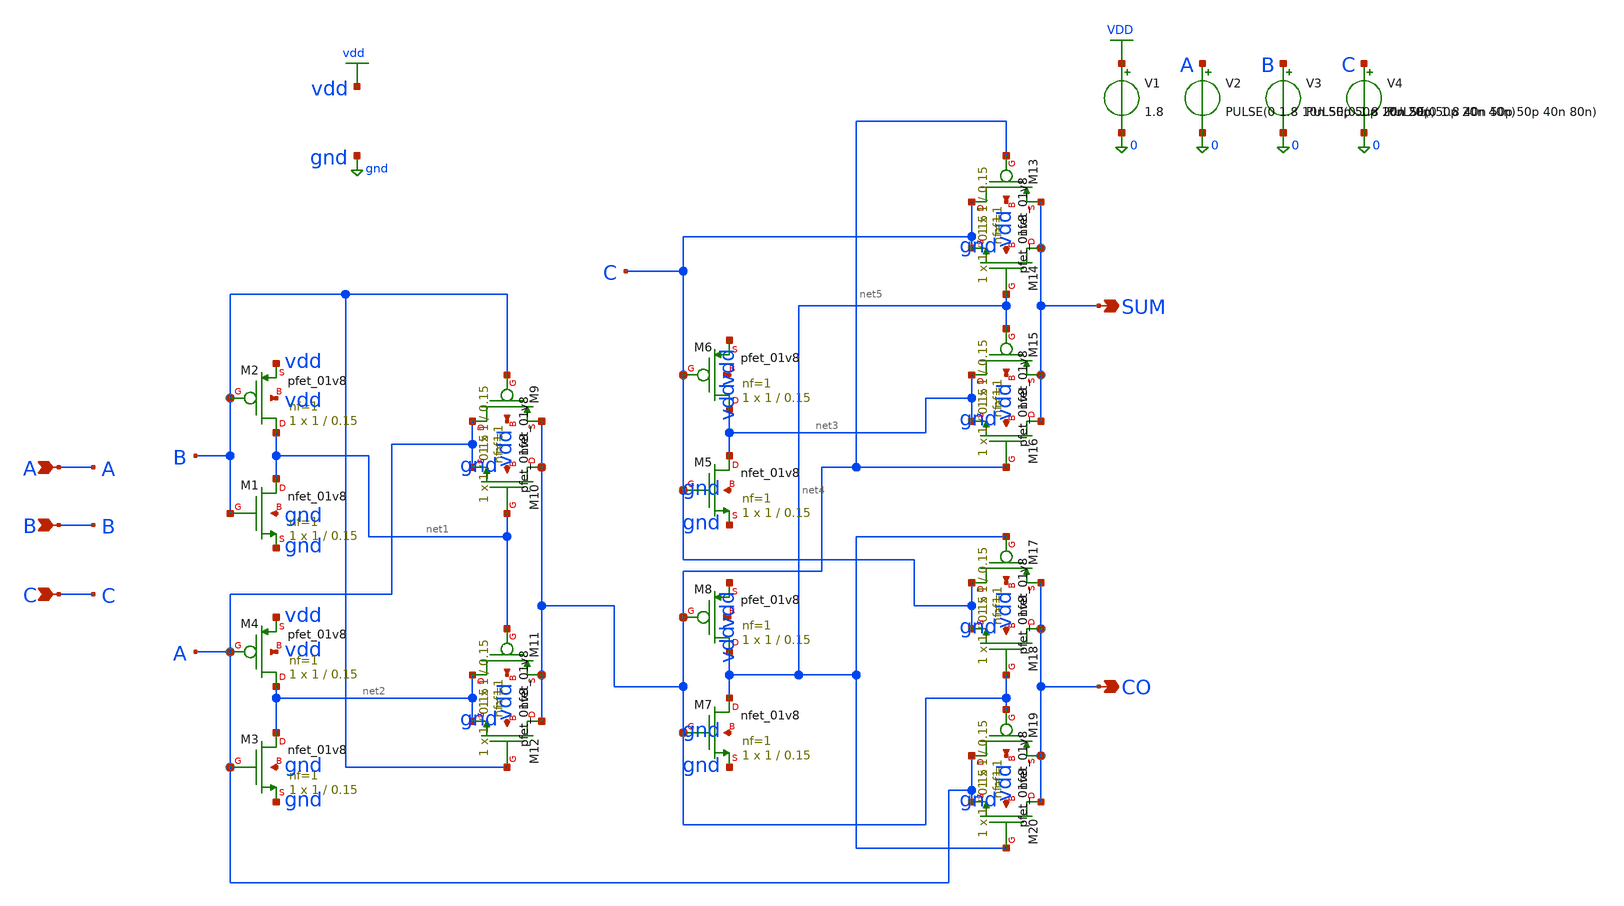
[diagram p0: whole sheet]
** sch_path: tb_FA20T.sch
**.subckt tb_FA20T A B C SUM CO
*.ipin A
*.ipin B
*.ipin C
*.opin SUM
*.opin CO
XM1 net1 B gnd gnd sky130_fd_pr__nfet_01v8 L=0.15 W=1 nf=1 ad='int((1 + 1)/2) * 1 / 1 * 0.29' as='int((1 + 2)/2) * 1 / 1 * 0.29'
+ pd='2*int((1 + 1)/2) * (1 / 1 + 0.29)' ps='2*int((1 + 2)/2) * (1 / 1 + 0.29)' nrd='0.29 / 1 ' nrs='0.29 / 1 '
+ sa=0 sb=0 sd=0 mult=1 m=1
XM2 net1 B vdd vdd sky130_fd_pr__pfet_01v8 L=0.15 W=1 nf=1 ad='int((1 + 1)/2) * 1 / 1 * 0.29' as='int((1 + 2)/2) * 1 / 1 * 0.29'
+ pd='2*int((1 + 1)/2) * (1 / 1 + 0.29)' ps='2*int((1 + 2)/2) * (1 / 1 + 0.29)' nrd='0.29 / 1 ' nrs='0.29 / 1 '
+ sa=0 sb=0 sd=0 mult=1 m=1
XM3 net2 A gnd gnd sky130_fd_pr__nfet_01v8 L=0.15 W=1 nf=1 ad='int((1 + 1)/2) * 1 / 1 * 0.29' as='int((1 + 2)/2) * 1 / 1 * 0.29'
+ pd='2*int((1 + 1)/2) * (1 / 1 + 0.29)' ps='2*int((1 + 2)/2) * (1 / 1 + 0.29)' nrd='0.29 / 1 ' nrs='0.29 / 1 '
+ sa=0 sb=0 sd=0 mult=1 m=1
XM4 net2 A vdd vdd sky130_fd_pr__pfet_01v8 L=0.15 W=1 nf=1 ad='int((1 + 1)/2) * 1 / 1 * 0.29' as='int((1 + 2)/2) * 1 / 1 * 0.29'
+ pd='2*int((1 + 1)/2) * (1 / 1 + 0.29)' ps='2*int((1 + 2)/2) * (1 / 1 + 0.29)' nrd='0.29 / 1 ' nrs='0.29 / 1 '
+ sa=0 sb=0 sd=0 mult=1 m=1
XM5 net3 C gnd gnd sky130_fd_pr__nfet_01v8 L=0.15 W=1 nf=1 ad='int((1 + 1)/2) * 1 / 1 * 0.29' as='int((1 + 2)/2) * 1 / 1 * 0.29'
+ pd='2*int((1 + 1)/2) * (1 / 1 + 0.29)' ps='2*int((1 + 2)/2) * (1 / 1 + 0.29)' nrd='0.29 / 1 ' nrs='0.29 / 1 '
+ sa=0 sb=0 sd=0 mult=1 m=1
XM6 net3 C vdd vdd sky130_fd_pr__pfet_01v8 L=0.15 W=1 nf=1 ad='int((1 + 1)/2) * 1 / 1 * 0.29' as='int((1 + 2)/2) * 1 / 1 * 0.29'
+ pd='2*int((1 + 1)/2) * (1 / 1 + 0.29)' ps='2*int((1 + 2)/2) * (1 / 1 + 0.29)' nrd='0.29 / 1 ' nrs='0.29 / 1 '
+ sa=0 sb=0 sd=0 mult=1 m=1
XM7 net4 net5 gnd gnd sky130_fd_pr__nfet_01v8 L=0.15 W=1 nf=1 ad='int((1 + 1)/2) * 1 / 1 * 0.29' as='int((1 + 2)/2) * 1 / 1 * 0.29'
+ pd='2*int((1 + 1)/2) * (1 / 1 + 0.29)' ps='2*int((1 + 2)/2) * (1 / 1 + 0.29)' nrd='0.29 / 1 ' nrs='0.29 / 1 '
+ sa=0 sb=0 sd=0 mult=1 m=1
XM8 net4 net5 vdd vdd sky130_fd_pr__pfet_01v8 L=0.15 W=1 nf=1 ad='int((1 + 1)/2) * 1 / 1 * 0.29' as='int((1 + 2)/2) * 1 / 1 * 0.29'
+ pd='2*int((1 + 1)/2) * (1 / 1 + 0.29)' ps='2*int((1 + 2)/2) * (1 / 1 + 0.29)' nrd='0.29 / 1 ' nrs='0.29 / 1 '
+ sa=0 sb=0 sd=0 mult=1 m=1
XM9 A B net5 vdd sky130_fd_pr__pfet_01v8 L=0.15 W=1 nf=1 ad='int((1 + 1)/2) * 1 / 1 * 0.29' as='int((1 + 2)/2) * 1 / 1 * 0.29'
+ pd='2*int((1 + 1)/2) * (1 / 1 + 0.29)' ps='2*int((1 + 2)/2) * (1 / 1 + 0.29)' nrd='0.29 / 1 ' nrs='0.29 / 1 '
+ sa=0 sb=0 sd=0 mult=1 m=1
XM10 net5 net1 A gnd sky130_fd_pr__nfet_01v8 L=0.15 W=1 nf=1 ad='int((1 + 1)/2) * 1 / 1 * 0.29' as='int((1 + 2)/2) * 1 / 1 * 0.29'
+ pd='2*int((1 + 1)/2) * (1 / 1 + 0.29)' ps='2*int((1 + 2)/2) * (1 / 1 + 0.29)' nrd='0.29 / 1 ' nrs='0.29 / 1 '
+ sa=0 sb=0 sd=0 mult=1 m=1
XM11 net2 net1 net5 vdd sky130_fd_pr__pfet_01v8 L=0.15 W=1 nf=1 ad='int((1 + 1)/2) * 1 / 1 * 0.29' as='int((1 + 2)/2) * 1 / 1 * 0.29'
+ pd='2*int((1 + 1)/2) * (1 / 1 + 0.29)' ps='2*int((1 + 2)/2) * (1 / 1 + 0.29)' nrd='0.29 / 1 ' nrs='0.29 / 1 '
+ sa=0 sb=0 sd=0 mult=1 m=1
XM12 net5 B net2 gnd sky130_fd_pr__nfet_01v8 L=0.15 W=1 nf=1 ad='int((1 + 1)/2) * 1 / 1 * 0.29' as='int((1 + 2)/2) * 1 / 1 * 0.29'
+ pd='2*int((1 + 1)/2) * (1 / 1 + 0.29)' ps='2*int((1 + 2)/2) * (1 / 1 + 0.29)' nrd='0.29 / 1 ' nrs='0.29 / 1 '
+ sa=0 sb=0 sd=0 mult=1 m=1
XM13 C net5 SUM vdd sky130_fd_pr__pfet_01v8 L=0.15 W=1 nf=1 ad='int((1 + 1)/2) * 1 / 1 * 0.29' as='int((1 + 2)/2) * 1 / 1 * 0.29'
+ pd='2*int((1 + 1)/2) * (1 / 1 + 0.29)' ps='2*int((1 + 2)/2) * (1 / 1 + 0.29)' nrd='0.29 / 1 ' nrs='0.29 / 1 '
+ sa=0 sb=0 sd=0 mult=1 m=1
XM14 SUM net4 C gnd sky130_fd_pr__nfet_01v8 L=0.15 W=1 nf=1 ad='int((1 + 1)/2) * 1 / 1 * 0.29' as='int((1 + 2)/2) * 1 / 1 * 0.29'
+ pd='2*int((1 + 1)/2) * (1 / 1 + 0.29)' ps='2*int((1 + 2)/2) * (1 / 1 + 0.29)' nrd='0.29 / 1 ' nrs='0.29 / 1 '
+ sa=0 sb=0 sd=0 mult=1 m=1
XM15 net3 net4 SUM vdd sky130_fd_pr__pfet_01v8 L=0.15 W=1 nf=1 ad='int((1 + 1)/2) * 1 / 1 * 0.29' as='int((1 + 2)/2) * 1 / 1 * 0.29'
+ pd='2*int((1 + 1)/2) * (1 / 1 + 0.29)' ps='2*int((1 + 2)/2) * (1 / 1 + 0.29)' nrd='0.29 / 1 ' nrs='0.29 / 1 '
+ sa=0 sb=0 sd=0 mult=1 m=1
XM16 SUM net5 net3 gnd sky130_fd_pr__nfet_01v8 L=0.15 W=1 nf=1 ad='int((1 + 1)/2) * 1 / 1 * 0.29' as='int((1 + 2)/2) * 1 / 1 * 0.29'
+ pd='2*int((1 + 1)/2) * (1 / 1 + 0.29)' ps='2*int((1 + 2)/2) * (1 / 1 + 0.29)' nrd='0.29 / 1 ' nrs='0.29 / 1 '
+ sa=0 sb=0 sd=0 mult=1 m=1
XM17 C net4 CO vdd sky130_fd_pr__pfet_01v8 L=0.15 W=1 nf=1 ad='int((1 + 1)/2) * 1 / 1 * 0.29' as='int((1 + 2)/2) * 1 / 1 * 0.29'
+ pd='2*int((1 + 1)/2) * (1 / 1 + 0.29)' ps='2*int((1 + 2)/2) * (1 / 1 + 0.29)' nrd='0.29 / 1 ' nrs='0.29 / 1 '
+ sa=0 sb=0 sd=0 mult=1 m=1
XM18 CO net5 C gnd sky130_fd_pr__nfet_01v8 L=0.15 W=1 nf=1 ad='int((1 + 1)/2) * 1 / 1 * 0.29' as='int((1 + 2)/2) * 1 / 1 * 0.29'
+ pd='2*int((1 + 1)/2) * (1 / 1 + 0.29)' ps='2*int((1 + 2)/2) * (1 / 1 + 0.29)' nrd='0.29 / 1 ' nrs='0.29 / 1 '
+ sa=0 sb=0 sd=0 mult=1 m=1
XM19 A net5 CO vdd sky130_fd_pr__pfet_01v8 L=0.15 W=1 nf=1 ad='int((1 + 1)/2) * 1 / 1 * 0.29' as='int((1 + 2)/2) * 1 / 1 * 0.29'
+ pd='2*int((1 + 1)/2) * (1 / 1 + 0.29)' ps='2*int((1 + 2)/2) * (1 / 1 + 0.29)' nrd='0.29 / 1 ' nrs='0.29 / 1 '
+ sa=0 sb=0 sd=0 mult=1 m=1
XM20 CO net4 A gnd sky130_fd_pr__nfet_01v8 L=0.15 W=1 nf=1 ad='int((1 + 1)/2) * 1 / 1 * 0.29' as='int((1 + 2)/2) * 1 / 1 * 0.29'
+ pd='2*int((1 + 1)/2) * (1 / 1 + 0.29)' ps='2*int((1 + 2)/2) * (1 / 1 + 0.29)' nrd='0.29 / 1 ' nrs='0.29 / 1 '
+ sa=0 sb=0 sd=0 mult=1 m=1
V1 VDD 0 1.8
V2 A 0 PULSE(0 1.8 10n 50p 50p 10n 20n)
V3 B 0 PULSE(0 1.8 20n 50p 50p 20n 40n)
V4 C 0 PULSE(0 1.8 40n 50p 50p 40n 80n)
**** begin user architecture code
.lib /foss/pdks/sky130A/libs.tech/ngspice/sky130.lib.spice tt

.control
save all
tran 50p 80n

plot v(A) v(B) v(C)
plot v(S) v(C0)
write /foss/designs/tb_FA20T.raw
.endc

.end

**** end user architecture code
**.ends
.GLOBAL VDD
.GLOBAL vdd
.GLOBAL gnd
.end
